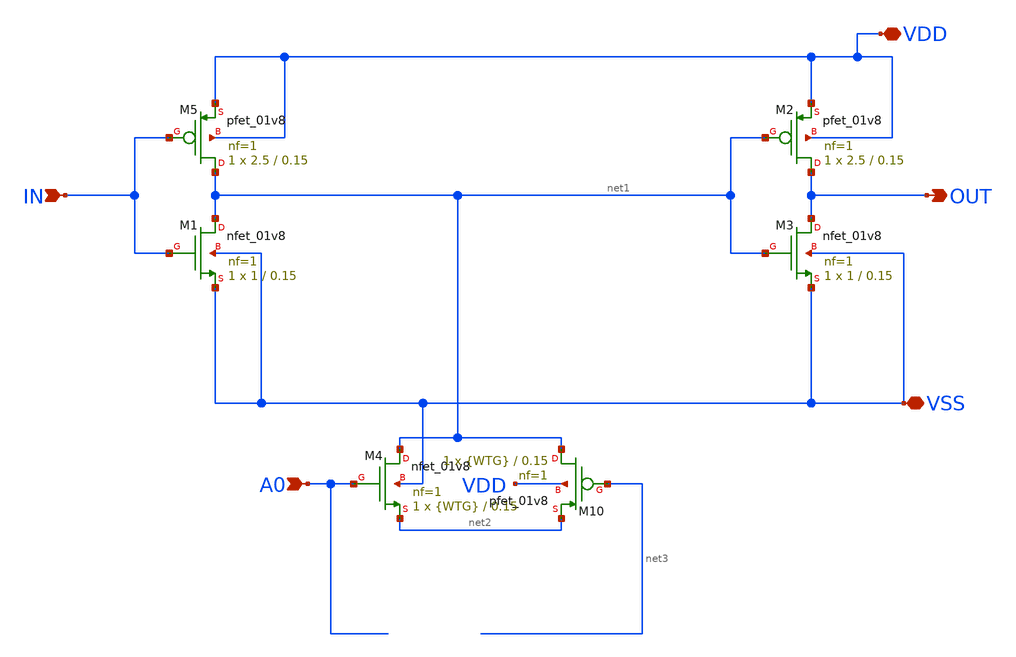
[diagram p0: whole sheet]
** sch_path: xschem/schematic/SCI_DCDL/TG_SCI/SCI_1bit.sch
**.subckt SCI_1bit IN OUT VDD VSS A0
*.ipin IN
*.opin OUT
*.iopin VDD
*.iopin VSS
*.ipin A0
XM1 net1 IN VSS VSS sky130_fd_pr__nfet_01v8 L=0.15 W=1 nf=1 ad='int((1 + 1)/2) * 1 / 1 * 0.29' as='int((1 + 2)/2) * 1 / 1 * 0.29'
+ pd='2*int((1 + 1)/2) * (1 / 1 + 0.29)' ps='2*int((1 + 2)/2) * (1 / 1 + 0.29)' nrd='0.29 / 1 ' nrs='0.29 / 1 '
+ sa=0 sb=0 sd=0 mult=1 m=1
XM3 OUT net1 VSS VSS sky130_fd_pr__nfet_01v8 L=0.15 W=1 nf=1 ad='int((1 + 1)/2) * 1 / 1 * 0.29' as='int((1 + 2)/2) * 1 / 1 * 0.29'
+ pd='2*int((1 + 1)/2) * (1 / 1 + 0.29)' ps='2*int((1 + 2)/2) * (1 / 1 + 0.29)' nrd='0.29 / 1 ' nrs='0.29 / 1 '
+ sa=0 sb=0 sd=0 mult=1 m=1
XM5 net1 IN VDD VDD sky130_fd_pr__pfet_01v8 L=0.15 W=2.5 nf=1 ad='int((1 + 1)/2) * 2.5 / 1 * 0.29' as='int((1 + 2)/2) * 2.5 / 1 * 0.29'
+ pd='2*int((1 + 1)/2) * (2.5 / 1 + 0.29)' ps='2*int((1 + 2)/2) * (2.5 / 1 + 0.29)' nrd='0.29 / 2.5 ' nrs='0.29 / 2.5 '
+ sa=0 sb=0 sd=0 mult=1 m=1
XM2 OUT net1 VDD VDD sky130_fd_pr__pfet_01v8 L=0.15 W=2.5 nf=1 ad='int((1 + 1)/2) * 2.5 / 1 * 0.29' as='int((1 + 2)/2) * 2.5 / 1 * 0.29'
+ pd='2*int((1 + 1)/2) * (2.5 / 1 + 0.29)' ps='2*int((1 + 2)/2) * (2.5 / 1 + 0.29)' nrd='0.29 / 2.5 ' nrs='0.29 / 2.5 '
+ sa=0 sb=0 sd=0 mult=1 m=1
XM4 net1 A0 net2 VSS sky130_fd_pr__nfet_01v8 L=0.15 W={WTG} nf=1 ad='int((1 + 1)/2) * {WTG} / 1 * 0.29'
+ as='int((1 + 2)/2) * {WTG} / 1 * 0.29' pd='2*int((1 + 1)/2) * ({WTG} / 1 + 0.29)' ps='2*int((1 + 2)/2) * ({WTG} / 1 + 0.29)'
+ nrd='0.29 / {WTG} ' nrs='0.29 / {WTG} ' sa=0 sb=0 sd=0 mult=1 m=1
XM10 net1 net3 net2 VDD sky130_fd_pr__pfet_01v8 L=0.15 W={WTG} nf=1 ad='int((1 + 1)/2) * {WTG} / 1 * 0.29'
+ as='int((1 + 2)/2) * {WTG} / 1 * 0.29' pd='2*int((1 + 1)/2) * ({WTG} / 1 + 0.29)' ps='2*int((1 + 2)/2) * ({WTG} / 1 + 0.29)'
+ nrd='0.29 / {WTG} ' nrs='0.29 / {WTG} ' sa=0 sb=0 sd=0 mult=1 m=1
**.ends
.end
